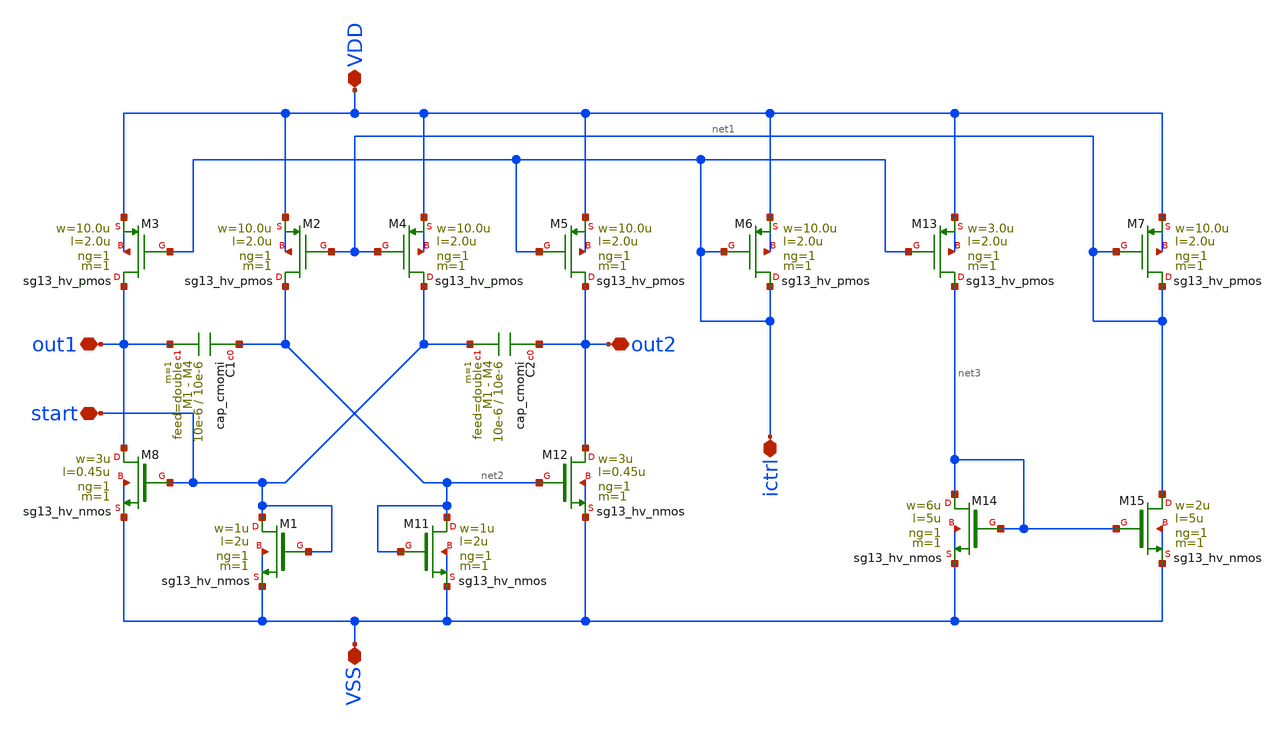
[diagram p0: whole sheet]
** sch_path: macros/heichips26_vcr/macros/switched_capacitor/schematic/xschem/osc.sch
**.subckt osc VSS VDD out2 out1 start ictrl
*.iopin VSS
*.iopin VDD
*.iopin out2
*.iopin out1
*.iopin start
*.iopin ictrl
XM3 out1 ictrl VDD VDD sg13_hv_pmos w=10.0u l=2.0u ng=1 m=1 mm_ok=1
XM2 net2 net1 VDD VDD sg13_hv_pmos w=10.0u l=2.0u ng=1 m=1 mm_ok=1
XM4 start net1 VDD VDD sg13_hv_pmos w=10.0u l=2.0u ng=1 m=1 mm_ok=1
XM5 out2 ictrl VDD VDD sg13_hv_pmos w=10.0u l=2.0u ng=1 m=1 mm_ok=1
XM6 ictrl ictrl VDD VDD sg13_hv_pmos w=10.0u l=2.0u ng=1 m=1 mm_ok=1
XM7 net1 net1 VDD VDD sg13_hv_pmos w=10.0u l=2.0u ng=1 m=1 mm_ok=1
XC1 net2 out1 cap_cmomi w=10e-6 l=10e-6 mmin=1 mmax=4 feed=double subblock=0 m=1 mm_ok=1
XC2 out2 start cap_cmomi w=10e-6 l=10e-6 mmin=1 mmax=4 feed=double subblock=0 m=1 mm_ok=1
XM8 out1 start VSS VSS sg13_hv_nmos w=3u l=0.45u ng=1 m=1 mm_ok=1
XM1 start start VSS VSS sg13_hv_nmos w=1u l=2u ng=1 m=1 mm_ok=1
XM12 out2 net2 VSS VSS sg13_hv_nmos w=3u l=0.45u ng=1 m=1 mm_ok=1
XM11 net2 net2 VSS VSS sg13_hv_nmos w=1u l=2u ng=1 m=1 mm_ok=1
XM13 net3 ictrl VDD VDD sg13_hv_pmos w=3.0u l=2.0u ng=1 m=1 mm_ok=1
XM14 net3 net3 VSS VSS sg13_hv_nmos w=6u l=5u ng=1 m=1 mm_ok=1
XM15 net1 net3 VSS VSS sg13_hv_nmos w=2u l=5u ng=1 m=1 mm_ok=1
**.ends
.end
